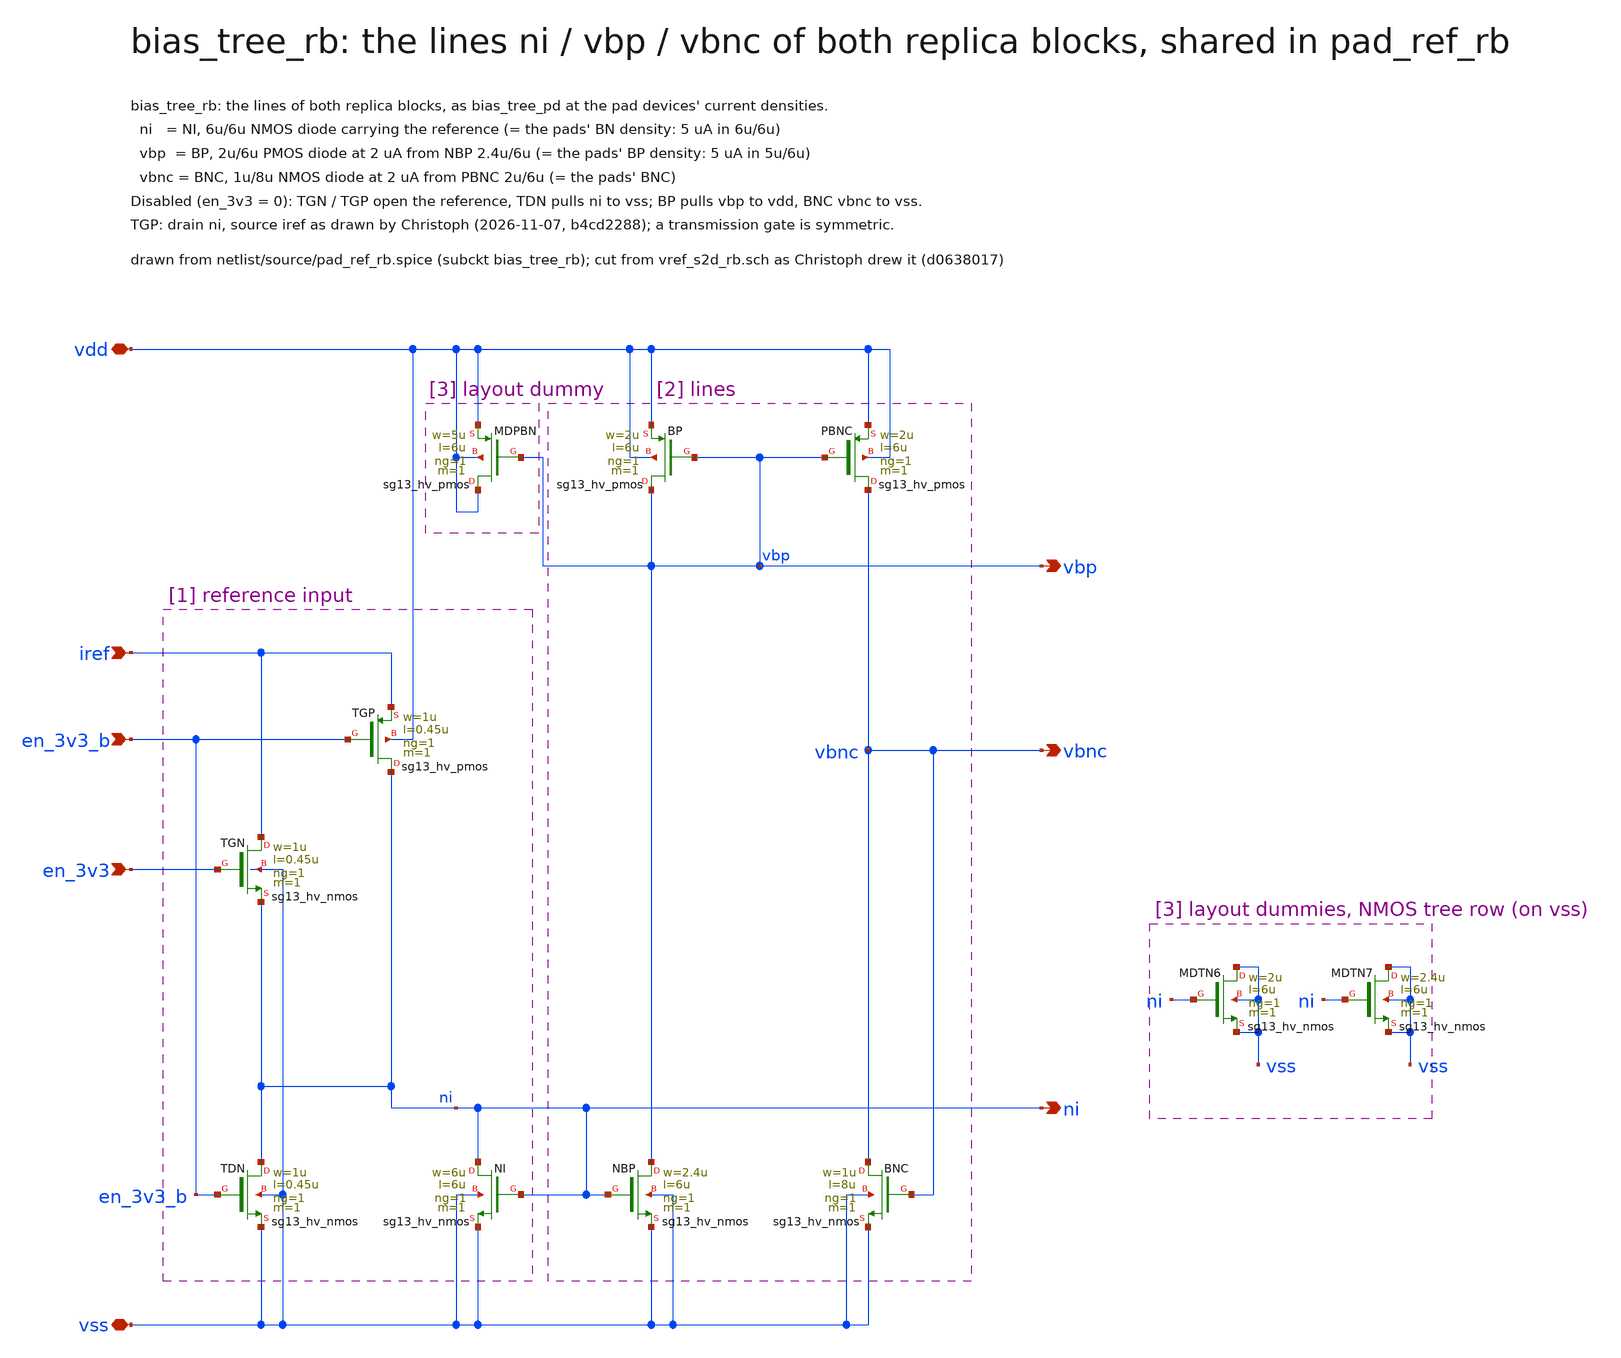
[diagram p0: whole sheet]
** sch_path: macros/pad_ref_rb/schematic/xschem/bias_tree_rb.sch
**.subckt bias_tree_rb vdd vss iref ni vbp vbnc en_3v3 en_3v3_b
*.iopin vdd
*.iopin vss
*.ipin iref
*.opin ni
*.opin vbp
*.opin vbnc
*.ipin en_3v3
*.ipin en_3v3_b
XMDTN6 vss ni vss vss sg13_hv_nmos w=2u l=6u ng=1 m=1 mm_ok=1
XMDTN7 vss ni vss vss sg13_hv_nmos w=2.4u l=6u ng=1 m=1 mm_ok=1
XTGN iref en_3v3 ni vss sg13_hv_nmos w=1u l=0.45u ng=1 m=1 mm_ok=1
XTGP ni en_3v3_b iref vdd sg13_hv_pmos w=1u l=0.45u ng=1 m=1 mm_ok=1
XTDN ni en_3v3_b vss vss sg13_hv_nmos w=1u l=0.45u ng=1 m=1 mm_ok=1
XNI ni ni vss vss sg13_hv_nmos w=6u l=6u ng=1 m=1 mm_ok=1
XNBP vbp ni vss vss sg13_hv_nmos w=2.4u l=6u ng=1 m=1 mm_ok=1
XBP vbp vbp vdd vdd sg13_hv_pmos w=2u l=6u ng=1 m=1 mm_ok=1
XPBNC vbnc vbp vdd vdd sg13_hv_pmos w=2u l=6u ng=1 m=1 mm_ok=1
XBNC vbnc vbnc vss vss sg13_hv_nmos w=1u l=8u ng=1 m=1 mm_ok=1
XMDPBN vdd vbp vdd vdd sg13_hv_pmos w=5u l=6u ng=1 m=1 mm_ok=1
**.ends
.end
